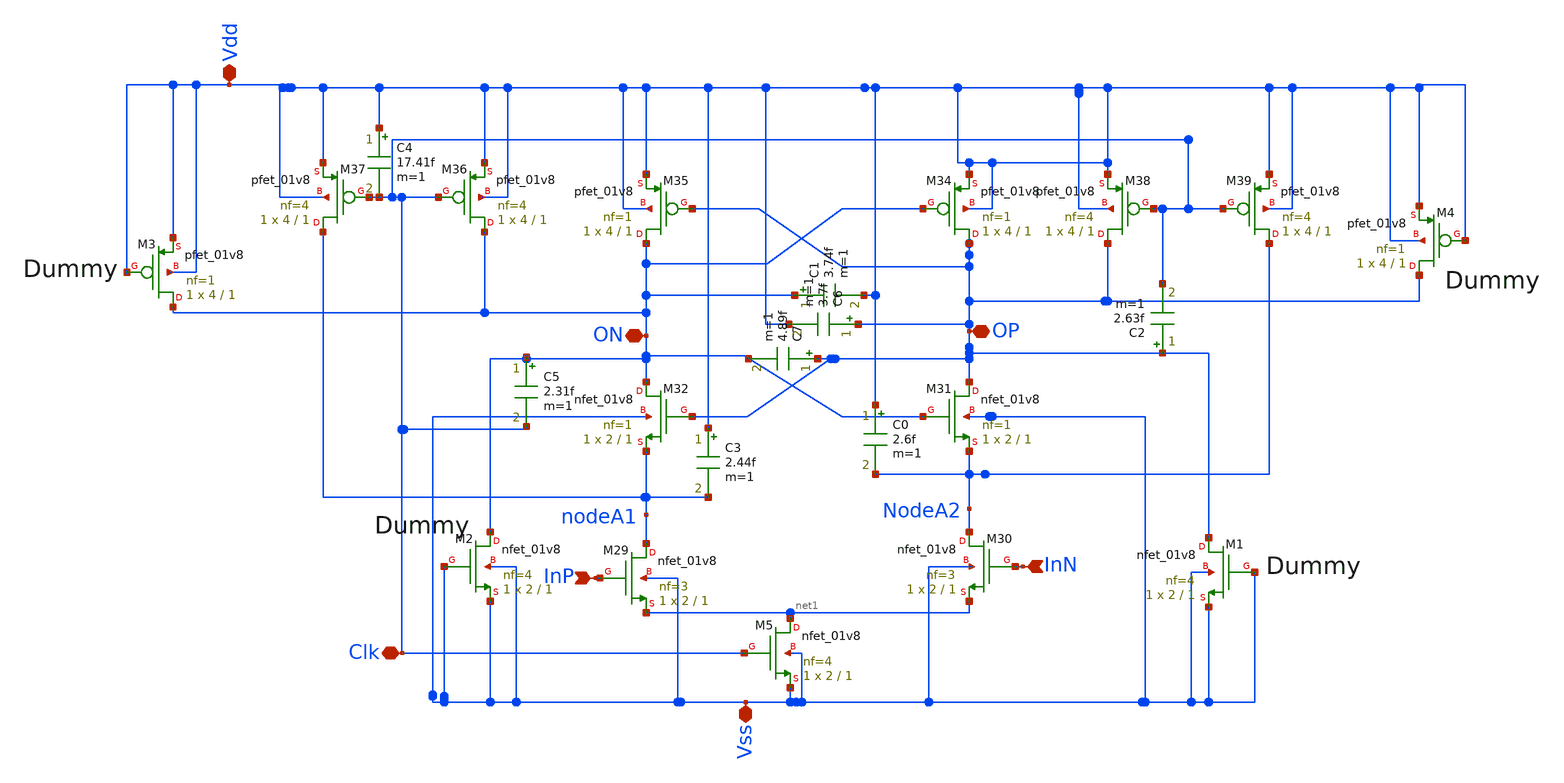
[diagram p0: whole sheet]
** sch_path: Quantizer/quantizer.sch
**.subckt quantizer Vss Vdd Clk InP InN ON OP
*.iopin Vss
*.iopin Vdd
*.iopin Clk
*.ipin InP
*.ipin InN
*.iopin ON
*.iopin OP
XM29 nodeA1 InP net1 Vss sky130_fd_pr__nfet_01v8 L=1 W=2 nf=3 ad='int((nf+1)/2) * W/nf * 0.29' as='int((nf+2)/2) * W/nf * 0.29'
+ pd='2*int((nf+1)/2) * (W/nf + 0.29)' ps='2*int((nf+2)/2) * (W/nf + 0.29)' nrd='0.29 / W' nrs='0.29 / W'
+ sa=0 sb=0 sd=0 mult=1 m=1
XM30 NodeA2 InN net1 Vss sky130_fd_pr__nfet_01v8 L=1 W=2 nf=3 ad='int((nf+1)/2) * W/nf * 0.29' as='int((nf+2)/2) * W/nf * 0.29'
+ pd='2*int((nf+1)/2) * (W/nf + 0.29)' ps='2*int((nf+2)/2) * (W/nf + 0.29)' nrd='0.29 / W' nrs='0.29 / W'
+ sa=0 sb=0 sd=0 mult=1 m=1
XM31 OP ON NodeA2 Vss sky130_fd_pr__nfet_01v8 L=1 W=2 nf=1 ad='int((nf+1)/2) * W/nf * 0.29' as='int((nf+2)/2) * W/nf * 0.29'
+ pd='2*int((nf+1)/2) * (W/nf + 0.29)' ps='2*int((nf+2)/2) * (W/nf + 0.29)' nrd='0.29 / W' nrs='0.29 / W'
+ sa=0 sb=0 sd=0 mult=1 m=1
XM32 ON OP nodeA1 Vss sky130_fd_pr__nfet_01v8 L=1 W=2 nf=1 ad='int((nf+1)/2) * W/nf * 0.29' as='int((nf+2)/2) * W/nf * 0.29'
+ pd='2*int((nf+1)/2) * (W/nf + 0.29)' ps='2*int((nf+2)/2) * (W/nf + 0.29)' nrd='0.29 / W' nrs='0.29 / W'
+ sa=0 sb=0 sd=0 mult=1 m=1
XM34 OP ON Vdd Vdd sky130_fd_pr__pfet_01v8 L=1 W=4 nf=1 ad='int((nf+1)/2) * W/nf * 0.29' as='int((nf+2)/2) * W/nf * 0.29'
+ pd='2*int((nf+1)/2) * (W/nf + 0.29)' ps='2*int((nf+2)/2) * (W/nf + 0.29)' nrd='0.29 / W' nrs='0.29 / W'
+ sa=0 sb=0 sd=0 mult=1 m=1
XM35 ON OP Vdd Vdd sky130_fd_pr__pfet_01v8 L=1 W=4 nf=1 ad='int((nf+1)/2) * W/nf * 0.29' as='int((nf+2)/2) * W/nf * 0.29'
+ pd='2*int((nf+1)/2) * (W/nf + 0.29)' ps='2*int((nf+2)/2) * (W/nf + 0.29)' nrd='0.29 / W' nrs='0.29 / W'
+ sa=0 sb=0 sd=0 mult=1 m=1
XM36 ON Clk Vdd Vdd sky130_fd_pr__pfet_01v8 L=1 W=4 nf=4 ad='int((nf+1)/2) * W/nf * 0.29' as='int((nf+2)/2) * W/nf * 0.29'
+ pd='2*int((nf+1)/2) * (W/nf + 0.29)' ps='2*int((nf+2)/2) * (W/nf + 0.29)' nrd='0.29 / W' nrs='0.29 / W'
+ sa=0 sb=0 sd=0 mult=1 m=1
XM37 nodeA1 Clk Vdd Vdd sky130_fd_pr__pfet_01v8 L=1 W=4 nf=4 ad='int((nf+1)/2) * W/nf * 0.29' as='int((nf+2)/2) * W/nf * 0.29'
+ pd='2*int((nf+1)/2) * (W/nf + 0.29)' ps='2*int((nf+2)/2) * (W/nf + 0.29)' nrd='0.29 / W' nrs='0.29 / W'
+ sa=0 sb=0 sd=0 mult=1 m=1
XM38 OP Clk Vdd Vdd sky130_fd_pr__pfet_01v8 L=1 W=4 nf=4 ad='int((nf+1)/2) * W/nf * 0.29' as='int((nf+2)/2) * W/nf * 0.29'
+ pd='2*int((nf+1)/2) * (W/nf + 0.29)' ps='2*int((nf+2)/2) * (W/nf + 0.29)' nrd='0.29 / W' nrs='0.29 / W'
+ sa=0 sb=0 sd=0 mult=1 m=1
XM39 NodeA2 Clk Vdd Vdd sky130_fd_pr__pfet_01v8 L=1 W=4 nf=4 ad='int((nf+1)/2) * W/nf * 0.29' as='int((nf+2)/2) * W/nf * 0.29'
+ pd='2*int((nf+1)/2) * (W/nf + 0.29)' ps='2*int((nf+2)/2) * (W/nf + 0.29)' nrd='0.29 / W' nrs='0.29 / W'
+ sa=0 sb=0 sd=0 mult=1 m=1
XM1 OP Vss Vss Vss sky130_fd_pr__nfet_01v8 L=1 W=2 nf=4 ad='int((nf+1)/2) * W/nf * 0.29' as='int((nf+2)/2) * W/nf * 0.29'
+ pd='2*int((nf+1)/2) * (W/nf + 0.29)' ps='2*int((nf+2)/2) * (W/nf + 0.29)' nrd='0.29 / W' nrs='0.29 / W'
+ sa=0 sb=0 sd=0 mult=1 m=1
XM2 ON Vss Vss Vss sky130_fd_pr__nfet_01v8 L=1 W=2 nf=4 ad='int((nf+1)/2) * W/nf * 0.29' as='int((nf+2)/2) * W/nf * 0.29'
+ pd='2*int((nf+1)/2) * (W/nf + 0.29)' ps='2*int((nf+2)/2) * (W/nf + 0.29)' nrd='0.29 / W' nrs='0.29 / W'
+ sa=0 sb=0 sd=0 mult=1 m=1
XM3 ON Vdd Vdd Vdd sky130_fd_pr__pfet_01v8 L=1 W=4 nf=1 ad='int((nf+1)/2) * W/nf * 0.29' as='int((nf+2)/2) * W/nf * 0.29'
+ pd='2*int((nf+1)/2) * (W/nf + 0.29)' ps='2*int((nf+2)/2) * (W/nf + 0.29)' nrd='0.29 / W' nrs='0.29 / W'
+ sa=0 sb=0 sd=0 mult=1 m=1
XM4 OP Vdd Vdd Vdd sky130_fd_pr__pfet_01v8 L=1 W=4 nf=1 ad='int((nf+1)/2) * W/nf * 0.29' as='int((nf+2)/2) * W/nf * 0.29'
+ pd='2*int((nf+1)/2) * (W/nf + 0.29)' ps='2*int((nf+2)/2) * (W/nf + 0.29)' nrd='0.29 / W' nrs='0.29 / W'
+ sa=0 sb=0 sd=0 mult=1 m=1
XM5 net1 Clk Vss Vss sky130_fd_pr__nfet_01v8 L=1 W=2 nf=4 ad='int((nf+1)/2) * W/nf * 0.29' as='int((nf+2)/2) * W/nf * 0.29'
+ pd='2*int((nf+1)/2) * (W/nf + 0.29)' ps='2*int((nf+2)/2) * (W/nf + 0.29)' nrd='0.29 / W' nrs='0.29 / W'
+ sa=0 sb=0 sd=0 mult=1 m=1
C1 ON Vdd 3.74f m=1
C3 Vdd nodeA1 2.44f m=1
C0 Vdd NodeA2 2.6f m=1
C6 OP Vdd 3.7f m=1
C4 Vdd Clk 17.41f m=1
C2 OP Clk 2.63f m=1
C5 ON Clk 2.31f m=1
C7 OP net2 4.89f m=1
**.ends
.end
